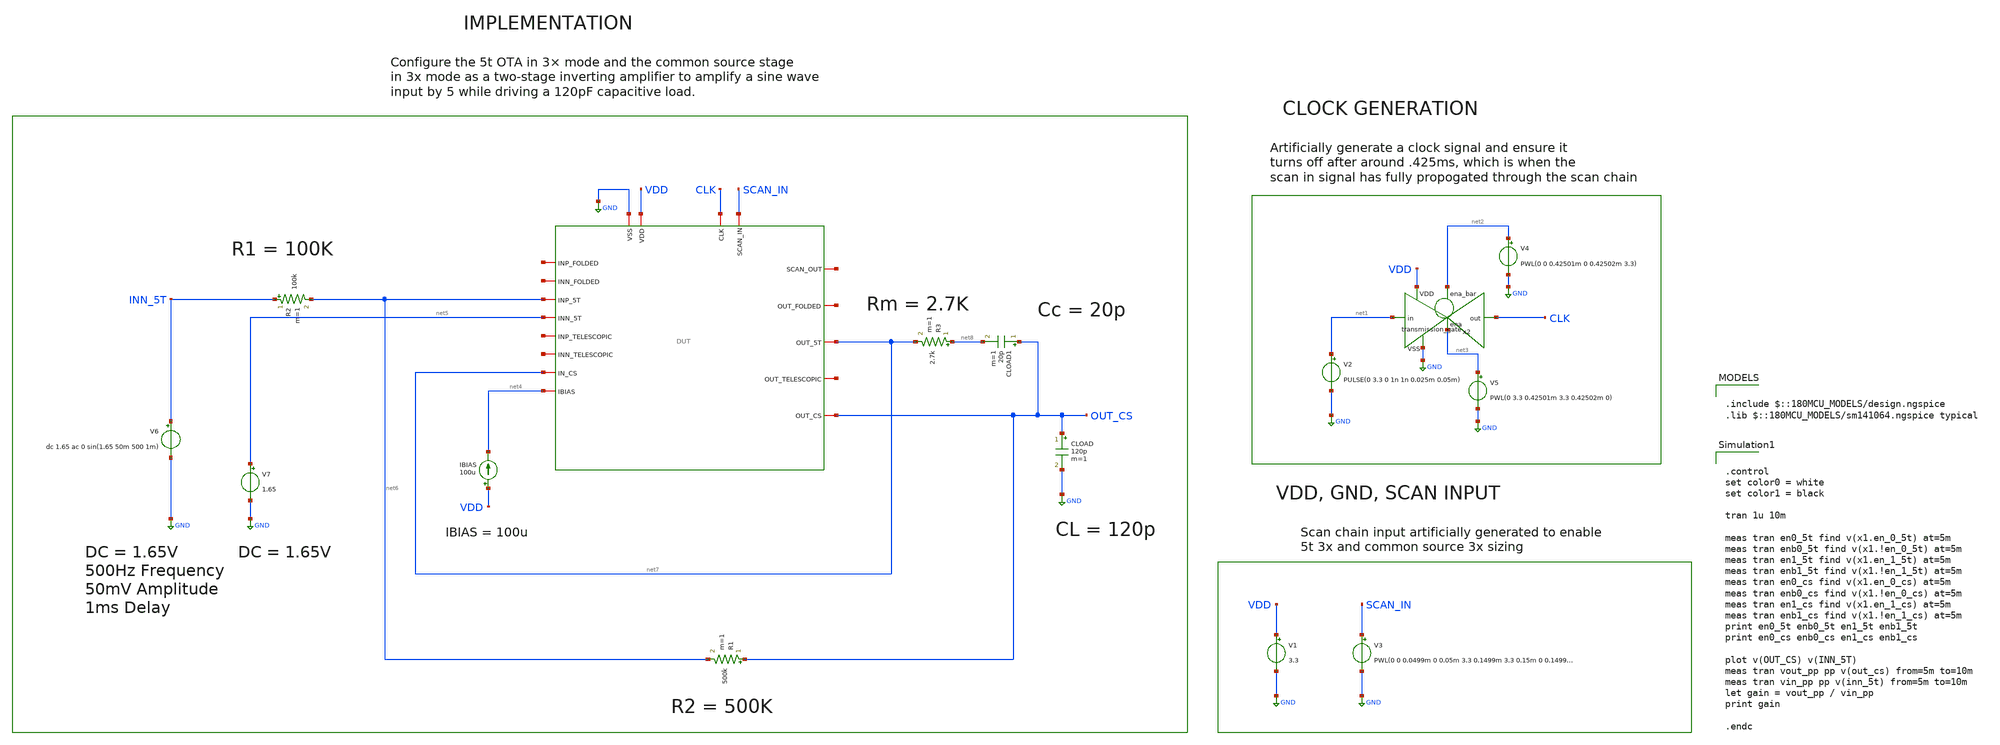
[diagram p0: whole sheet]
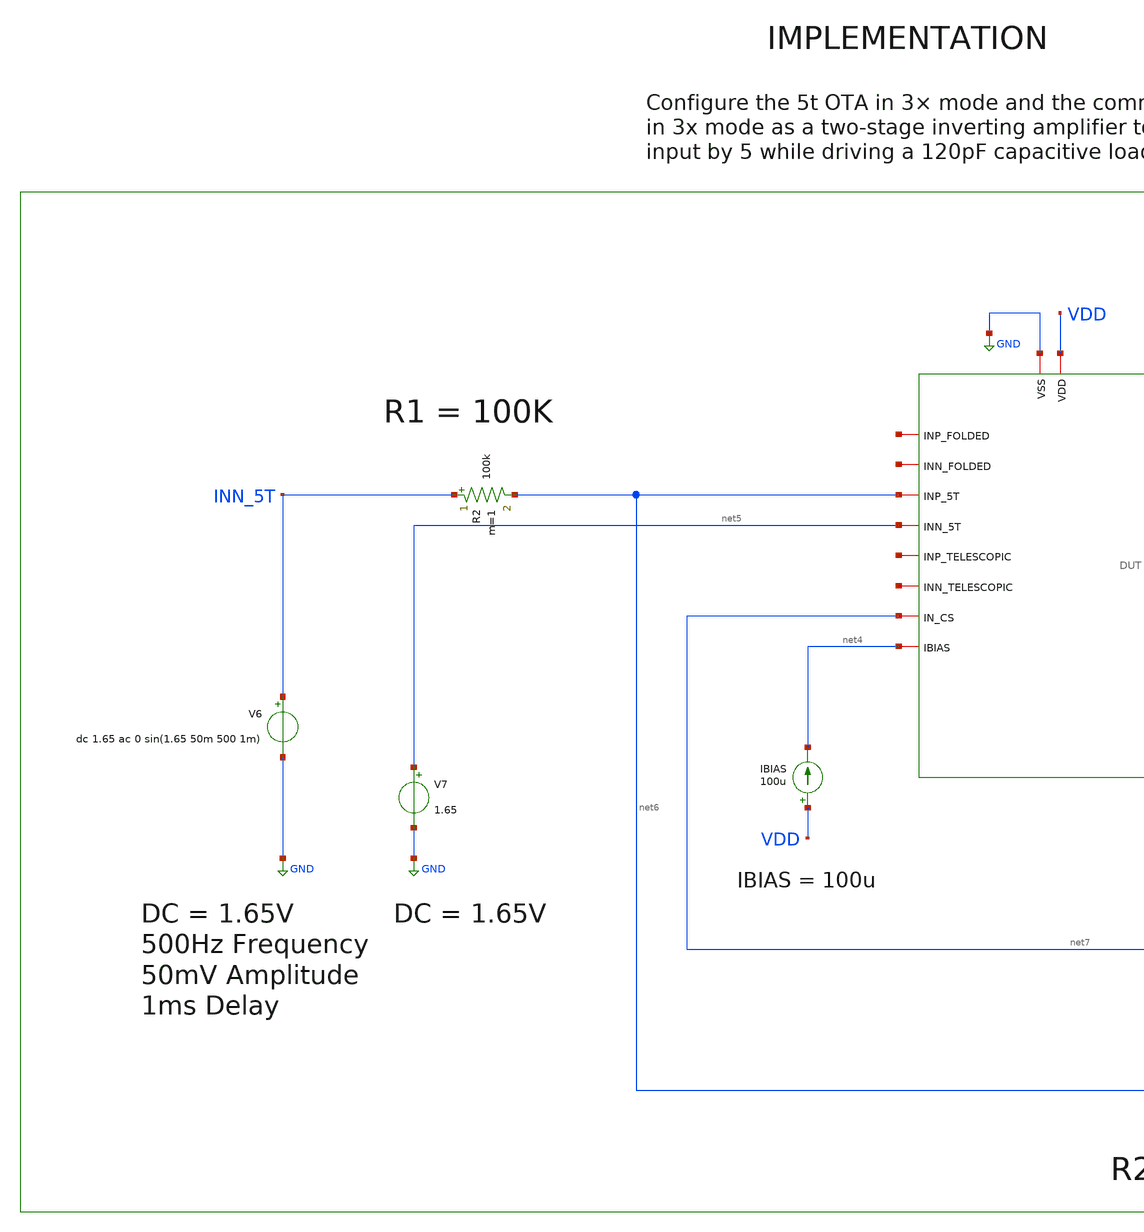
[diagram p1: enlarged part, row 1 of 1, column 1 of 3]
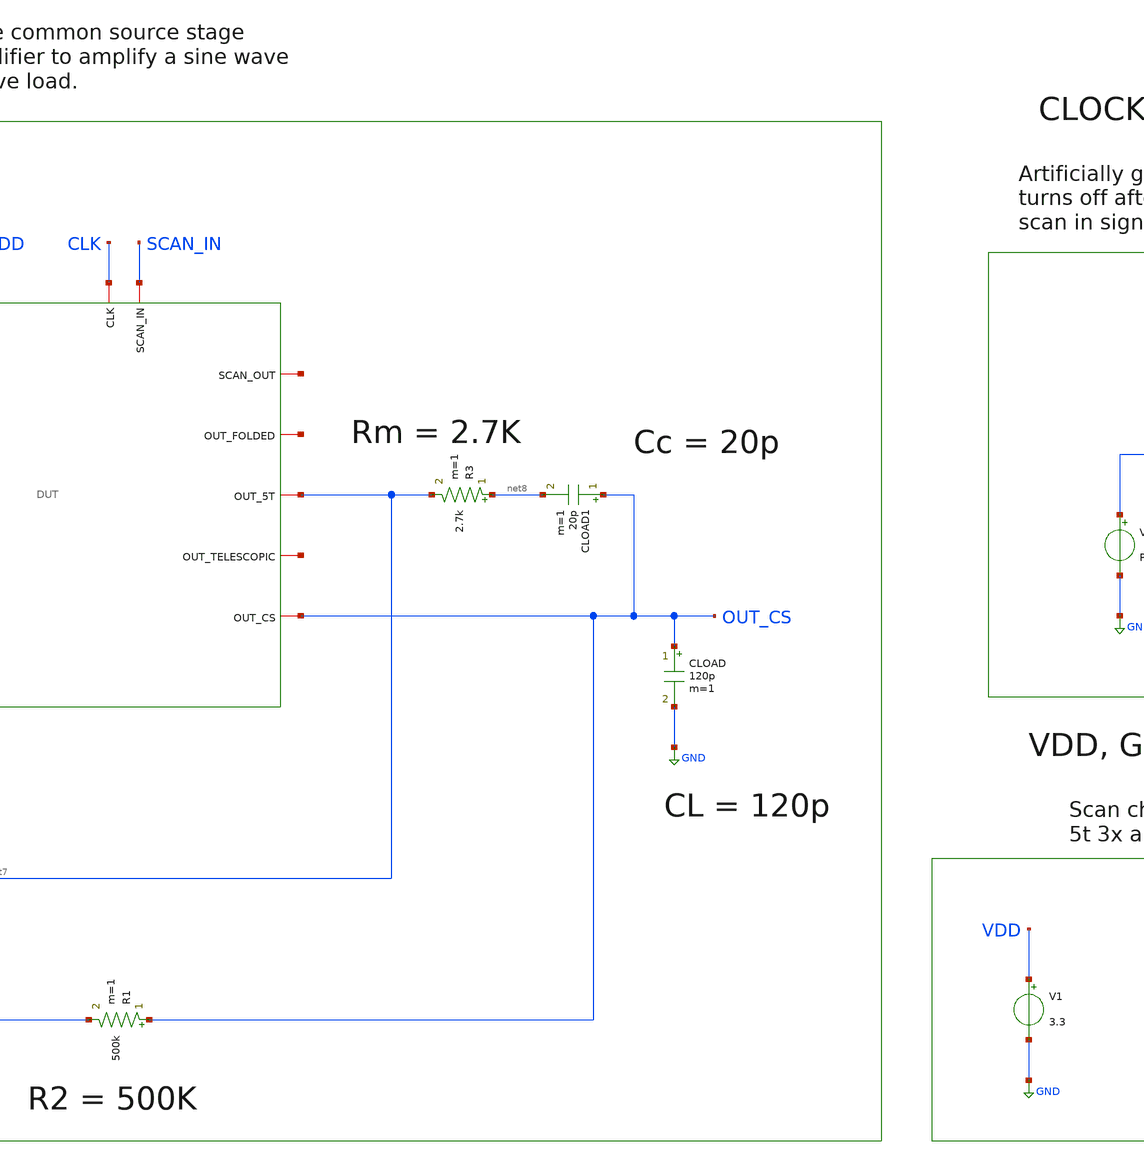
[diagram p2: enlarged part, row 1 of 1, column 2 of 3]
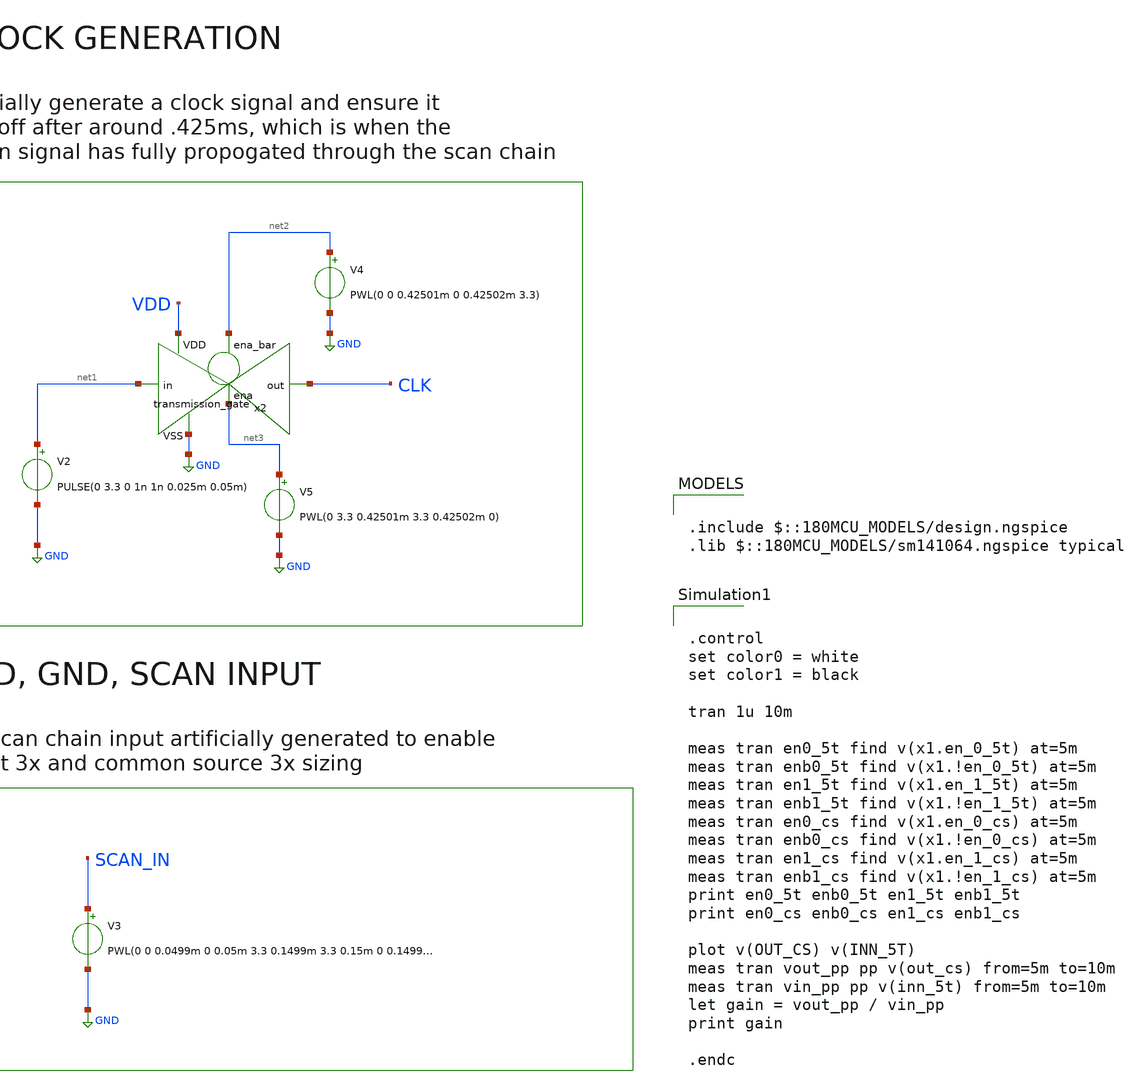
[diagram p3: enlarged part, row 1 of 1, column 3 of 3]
** sch_path: designs/libs/core_tb/sl/ota_5t/two_stage/5t_inverting_cs_3x.sch
**.subckt 5t_inverting_cs_3x
V3 SCAN_IN GND PWL(0 0 0.0499m 0 0.05m 3.3 0.1499m 3.3 0.15m 0 0.1499m 0 0.15m 3.3 0.24999m 3.3
+ 0.25m 0)
V1 VDD GND 3.3
V2 net1 GND PULSE(0 3.3 0 1n 1n 0.025m 0.05m)
x2 net2 VDD CLK net1 GND net3 transmission_gate
V4 net2 GND PWL(0 0 0.42501m 0 0.42502m 3.3)
V5 net3 GND PWL(0 3.3 0.42501m 3.3 0.42502m 0)
IBIAS VDD net4 100u
CLOAD OUT_CS GND 120p m=1
R3 net8 net7 2.7k m=1
CLOAD1 OUT_CS net8 20p m=1
V7 net5 GND 1.65
R2 INN_5T net6 100k m=1
R1 OUT_CS net6 500k m=1
V6 INN_5T GND dc 1.65 ac 0 sin(1.65 50m 500 1m)
x1 CLK net9 SCAN_IN GND VDD net10 net11 net7 net4 net12 net6 net5 net13 net14 OUT_CS net7 net15 DUT
**** begin user architecture code

.include $::180MCU_MODELS/design.ngspice
.lib $::180MCU_MODELS/sm141064.ngspice typical



.control
set color0 = white
set color1 = black

tran 1u 10m

meas tran en0_5t find v(x1.en_0_5t) at=5m
meas tran enb0_5t find v(x1.!en_0_5t) at=5m
meas tran en1_5t find v(x1.en_1_5t) at=5m
meas tran enb1_5t find v(x1.!en_1_5t) at=5m
meas tran en0_cs find v(x1.en_0_cs) at=5m
meas tran enb0_cs find v(x1.!en_0_cs) at=5m
meas tran en1_cs find v(x1.en_1_cs) at=5m
meas tran enb1_cs find v(x1.!en_1_cs) at=5m
print en0_5t enb0_5t en1_5t enb1_5t
print en0_cs enb0_cs en1_cs enb1_cs

plot v(OUT_CS) v(INN_5T)
meas tran vout_pp pp v(out_cs) from=5m to=10m
meas tran vin_pp pp v(inn_5t) from=5m to=10m
let gain = vout_pp / vin_pp
print gain

.endc


**** end user architecture code
**.ends
.GLOBAL GND
.end
